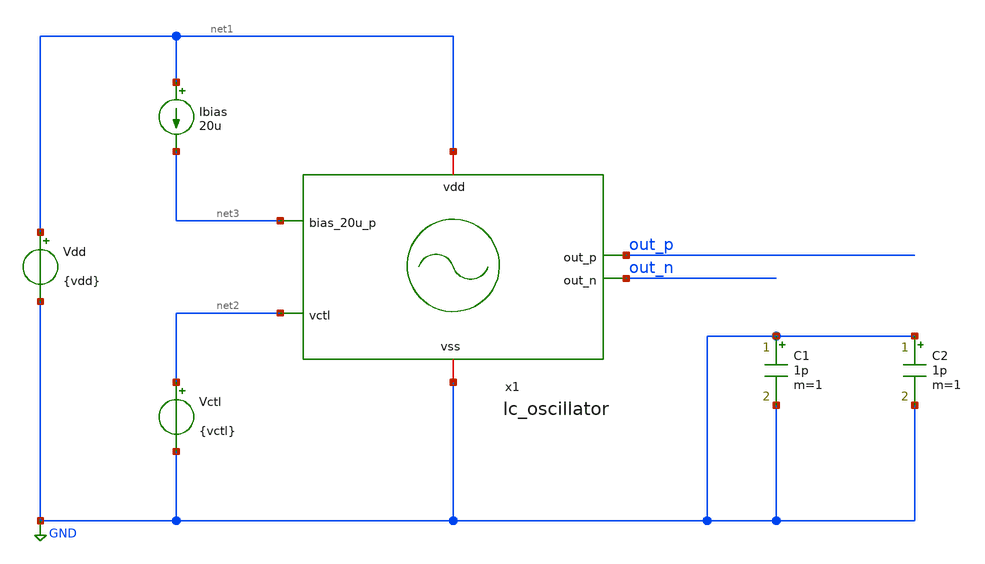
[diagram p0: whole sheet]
** sch_path: design/lc_oscillator/test/lc_oscillator_tb.sch
**.subckt lc_oscillator_tb
x1 net1 out_p net2 out_n net3 GND lc_oscillator
Ibias net1 net3 20u
Vctl net2 GND {vctl}
Vdd net1 GND {vdd}
C1 GND GND 1p m=1
C2 GND GND 1p m=1
**** begin user architecture code


.param temp=27

.param vdd=1.8 vctl=1.6

*.op
.tran 1p 300n uic

*.options rshunt=1e11

.save all




.options wnflag=1
.include $::SKYWATER_MODELS/cells/nfet_01v8/sky130_fd_pr__nfet_01v8__tt.corner.spice
.include $::SKYWATER_MODELS/cells/nfet_01v8_lvt/sky130_fd_pr__nfet_01v8_lvt__tt.corner.spice
.include $::SKYWATER_MODELS/cells/pfet_01v8/sky130_fd_pr__pfet_01v8__tt.corner.spice
.include $::SKYWATER_MODELS/cells/nfet_03v3_nvt/sky130_fd_pr__nfet_03v3_nvt__tt.corner.spice
.include $::SKYWATER_MODELS/cells/nfet_05v0_nvt/sky130_fd_pr__nfet_05v0_nvt__tt.corner.spice
.include $::SKYWATER_MODELS/cells/esd_nfet_01v8/sky130_fd_pr__esd_nfet_01v8__tt.corner.spice
.include $::SKYWATER_MODELS/cells/pfet_01v8_lvt/sky130_fd_pr__pfet_01v8_lvt__tt.corner.spice
.include $::SKYWATER_MODELS/cells/pfet_01v8_hvt/sky130_fd_pr__pfet_01v8_hvt__tt.corner.spice
.include $::SKYWATER_MODELS/cells/esd_pfet_g5v0d10v5/sky130_fd_pr__esd_pfet_g5v0d10v5__tt.corner.spice
.include $::SKYWATER_MODELS/cells/pfet_g5v0d10v5/sky130_fd_pr__pfet_g5v0d10v5__tt.corner.spice
.include $::SKYWATER_MODELS/cells/pfet_g5v0d16v0/sky130_fd_pr__pfet_g5v0d16v0__tt.corner.spice
.include $::SKYWATER_MODELS/cells/nfet_g5v0d10v5/sky130_fd_pr__nfet_g5v0d10v5__tt.corner.spice
.include $::SKYWATER_MODELS/cells/nfet_g5v0d16v0/sky130_fd_pr__nfet_g5v0d16v0__tt_discrete.corner.spice
.include $::SKYWATER_MODELS/cells/esd_nfet_g5v0d10v5/sky130_fd_pr__esd_nfet_g5v0d10v5__tt.corner.spice
.include $::SKYWATER_MODELS/models/corners/tt/nonfet.spice
* Mismatch parameters
.include $::SKYWATER_MODELS/cells/nfet_01v8/sky130_fd_pr__nfet_01v8__mismatch.corner.spice
.include $::SKYWATER_MODELS/cells/pfet_01v8/sky130_fd_pr__pfet_01v8__mismatch.corner.spice
.include $::SKYWATER_MODELS/cells/nfet_01v8_lvt/sky130_fd_pr__nfet_01v8_lvt__mismatch.corner.spice
.include $::SKYWATER_MODELS/cells/pfet_01v8_lvt/sky130_fd_pr__pfet_01v8_lvt__mismatch.corner.spice
.include $::SKYWATER_MODELS/cells/pfet_01v8_hvt/sky130_fd_pr__pfet_01v8_hvt__mismatch.corner.spice
.include $::SKYWATER_MODELS/cells/nfet_g5v0d10v5/sky130_fd_pr__nfet_g5v0d10v5__mismatch.corner.spice
.include $::SKYWATER_MODELS/cells/pfet_g5v0d10v5/sky130_fd_pr__pfet_g5v0d10v5__mismatch.corner.spice
.include $::SKYWATER_MODELS/cells/nfet_05v0_nvt/sky130_fd_pr__nfet_05v0_nvt__mismatch.corner.spice
.include $::SKYWATER_MODELS/cells/nfet_03v3_nvt/sky130_fd_pr__nfet_03v3_nvt__mismatch.corner.spice
* Resistor$::SKYWATER_MODELS/Capacitor
.include $::SKYWATER_MODELS/models/r+c/res_typical__cap_typical.spice
.include $::SKYWATER_MODELS/models/r+c/res_typical__cap_typical__lin.spice
* Special cells
.include $::SKYWATER_MODELS/models/corners/tt/specialized_cells.spice
* All models
.include $::SKYWATER_MODELS/models/all.spice
* Corner
.include $::SKYWATER_MODELS/models/corners/tt/rf.spice

 [sky130_models]
**** end user architecture code
**.ends

* expanding   symbol:  lc_oscillator/lc_oscillator.sym # of pins=6
** sym_path: design/lc_oscillator/lc_oscillator.sym
** sch_path: design/lc_oscillator/lc_oscillator.sch
.subckt lc_oscillator vdd out_p vctl out_n bias_20u_p vss
*.ipin vctl
*.iopin vss
*.ipin bias_20u_p
*.iopin vdd
*.opin out_p
*.opin out_n
x3 vdd out_p out_n vss lc_oscillator_inductor_diff
x4 vdd out_p vctl out_n bias_20u_p vss lc_oscillator_core
.ends


* expanding   symbol:  lc_oscillator_inductor_diff/lc_oscillator_inductor_diff.sym # of pins=4
** sym_path: design/lc_oscillator_inductor_diff/lc_oscillator_inductor_diff.sym
** sch_path: design/lc_oscillator_inductor_diff/lc_oscillator_inductor_diff.sch
.subckt lc_oscillator_inductor_diff common positive negative sub
*.iopin common
*.iopin positive
*.iopin sub
*.iopin negative
xlneg common negative sub lc_oscillator_inductor
xlpos common positive sub lc_oscillator_inductor
.ends


* expanding   symbol:  lc_oscillator_core/lc_oscillator_core.sym # of pins=6
** sym_path: design/lc_oscillator_core/lc_oscillator_core.sym
** sch_path: design/lc_oscillator_core/lc_oscillator_core.sch
.subckt lc_oscillator_core vdd ind_p vctl ind_n bias_20u_p vss
*.ipin vctl
*.iopin vss
*.ipin bias_20u_p
*.iopin vdd
*.iopin ind_n
*.iopin ind_p
XM2 bias_20u_p bias_20u_p vss vss sky130_fd_pr__nfet_01v8_lvt L=0.5 W=5 nf=1 ad='int((nf+1)/2) * W/nf * 0.29'
+ as='int((nf+2)/2) * W/nf * 0.29' pd='2*int((nf+1)/2) * (W/nf + 0.29)' ps='2*int((nf+2)/2) * (W/nf + 0.29)'
+ nrd='0.29 / W' nrs='0.29 / W' sa=0 sb=0 sd=0 mult=2 m=2
XM1 net3 bias_20u_p vss vss sky130_fd_pr__nfet_01v8_lvt L=0.5 W=5 nf=1 ad='int((nf+1)/2) * W/nf * 0.29'
+ as='int((nf+2)/2) * W/nf * 0.29' pd='2*int((nf+1)/2) * (W/nf + 0.29)' ps='2*int((nf+2)/2) * (W/nf + 0.29)'
+ nrd='0.29 / W' nrs='0.29 / W' sa=0 sb=0 sd=0 mult=32 m=32
XM3 net3 bias_20u_p vss vss sky130_fd_pr__nfet_01v8_lvt L=0.5 W=5 nf=1 ad='int((nf+1)/2) * W/nf * 0.29'
+ as='int((nf+2)/2) * W/nf * 0.29' pd='2*int((nf+1)/2) * (W/nf + 0.29)' ps='2*int((nf+2)/2) * (W/nf + 0.29)'
+ nrd='0.29 / W' nrs='0.29 / W' sa=0 sb=0 sd=0 mult=32 m=32
XC1 ind_p net2 sky130_fd_pr__cap_mim_m3_1 W=6 L=6 MF=4 m=4
XC2 ind_n net1 sky130_fd_pr__cap_mim_m3_1 W=6 L=6 MF=4 m=4
XC3 net2 net4 sky130_fd_pr__cap_mim_m3_1 W=6 L=6 MF=1 m=1
XC4 net1 net4 sky130_fd_pr__cap_mim_m3_1 W=6 L=6 MF=1 m=1
XM4 ind_p vdd net2 vss sky130_fd_pr__nfet_01v8_lvt L=0.15 W=40 nf=8 ad='int((nf+1)/2) * W/nf * 0.29'
+ as='int((nf+2)/2) * W/nf * 0.29' pd='2*int((nf+1)/2) * (W/nf + 0.29)' ps='2*int((nf+2)/2) * (W/nf + 0.29)'
+ nrd='0.29 / W' nrs='0.29 / W' sa=0 sb=0 sd=0 mult=1 m=1
XM5 ind_n vdd net1 vss sky130_fd_pr__nfet_01v8_lvt L=0.15 W=40 nf=8 ad='int((nf+1)/2) * W/nf * 0.29'
+ as='int((nf+2)/2) * W/nf * 0.29' pd='2*int((nf+1)/2) * (W/nf + 0.29)' ps='2*int((nf+2)/2) * (W/nf + 0.29)'
+ nrd='0.29 / W' nrs='0.29 / W' sa=0 sb=0 sd=0 mult=1 m=1
XM6 net2 net1 net3 vss sky130_fd_pr__nfet_01v8_lvt L=0.15 W=40 nf=8 ad='int((nf+1)/2) * W/nf * 0.29'
+ as='int((nf+2)/2) * W/nf * 0.29' pd='2*int((nf+1)/2) * (W/nf + 0.29)' ps='2*int((nf+2)/2) * (W/nf + 0.29)'
+ nrd='0.29 / W' nrs='0.29 / W' sa=0 sb=0 sd=0 mult=1 m=1
XM7 net1 net2 net3 vss sky130_fd_pr__nfet_01v8_lvt L=0.15 W=40 nf=8 ad='int((nf+1)/2) * W/nf * 0.29'
+ as='int((nf+2)/2) * W/nf * 0.29' pd='2*int((nf+1)/2) * (W/nf + 0.29)' ps='2*int((nf+2)/2) * (W/nf + 0.29)'
+ nrd='0.29 / W' nrs='0.29 / W' sa=0 sb=0 sd=0 mult=1 m=1
x1 vctl ind_p lc_oscillator_varactor
x2 vctl ind_n lc_oscillator_varactor
.ends


* expanding   symbol:  lc_oscillator_inductor/lc_oscillator_inductor.sym # of pins=3
** sym_path: design/lc_oscillator_inductor/lc_oscillator_inductor.sym
** sch_path: design/lc_oscillator_inductor/lc_oscillator_inductor.sch
.subckt lc_oscillator_inductor p1 p2 sub
*.iopin p2
*.iopin p1
*.iopin sub
L1 net1 p1 1.028n m=1
C1 p1 net2 62.02f m=1
R1 net2 sub 16.03 m=1
C2 p1 p2 0.1f m=1
C3 p2 net3 62.31f m=1
R2 net3 sub 15.88 m=1
R3 p2 net1 3.6825 m=1
.ends


* expanding   symbol:  lc_oscillator_varactor/lc_oscillator_varactor.sym # of pins=2
** sym_path: design/lc_oscillator_varactor/lc_oscillator_varactor.sym
** sch_path: design/lc_oscillator_varactor/lc_oscillator_varactor.sch
.subckt lc_oscillator_varactor p m
*.iopin p
*.iopin m
XM1 p m p p sky130_fd_pr__pfet_01v8 L=4 W=4 nf=1 ad='int((nf+1)/2) * W/nf * 0.29' as='int((nf+2)/2) * W/nf * 0.29'
+ pd='2*int((nf+1)/2) * (W/nf + 0.29)' ps='2*int((nf+2)/2) * (W/nf + 0.29)' nrd='0.29 / W' nrs='0.29 / W'
+ sa=0 sb=0 sd=0 mult=1 m=1
.ends

.GLOBAL GND
.end
